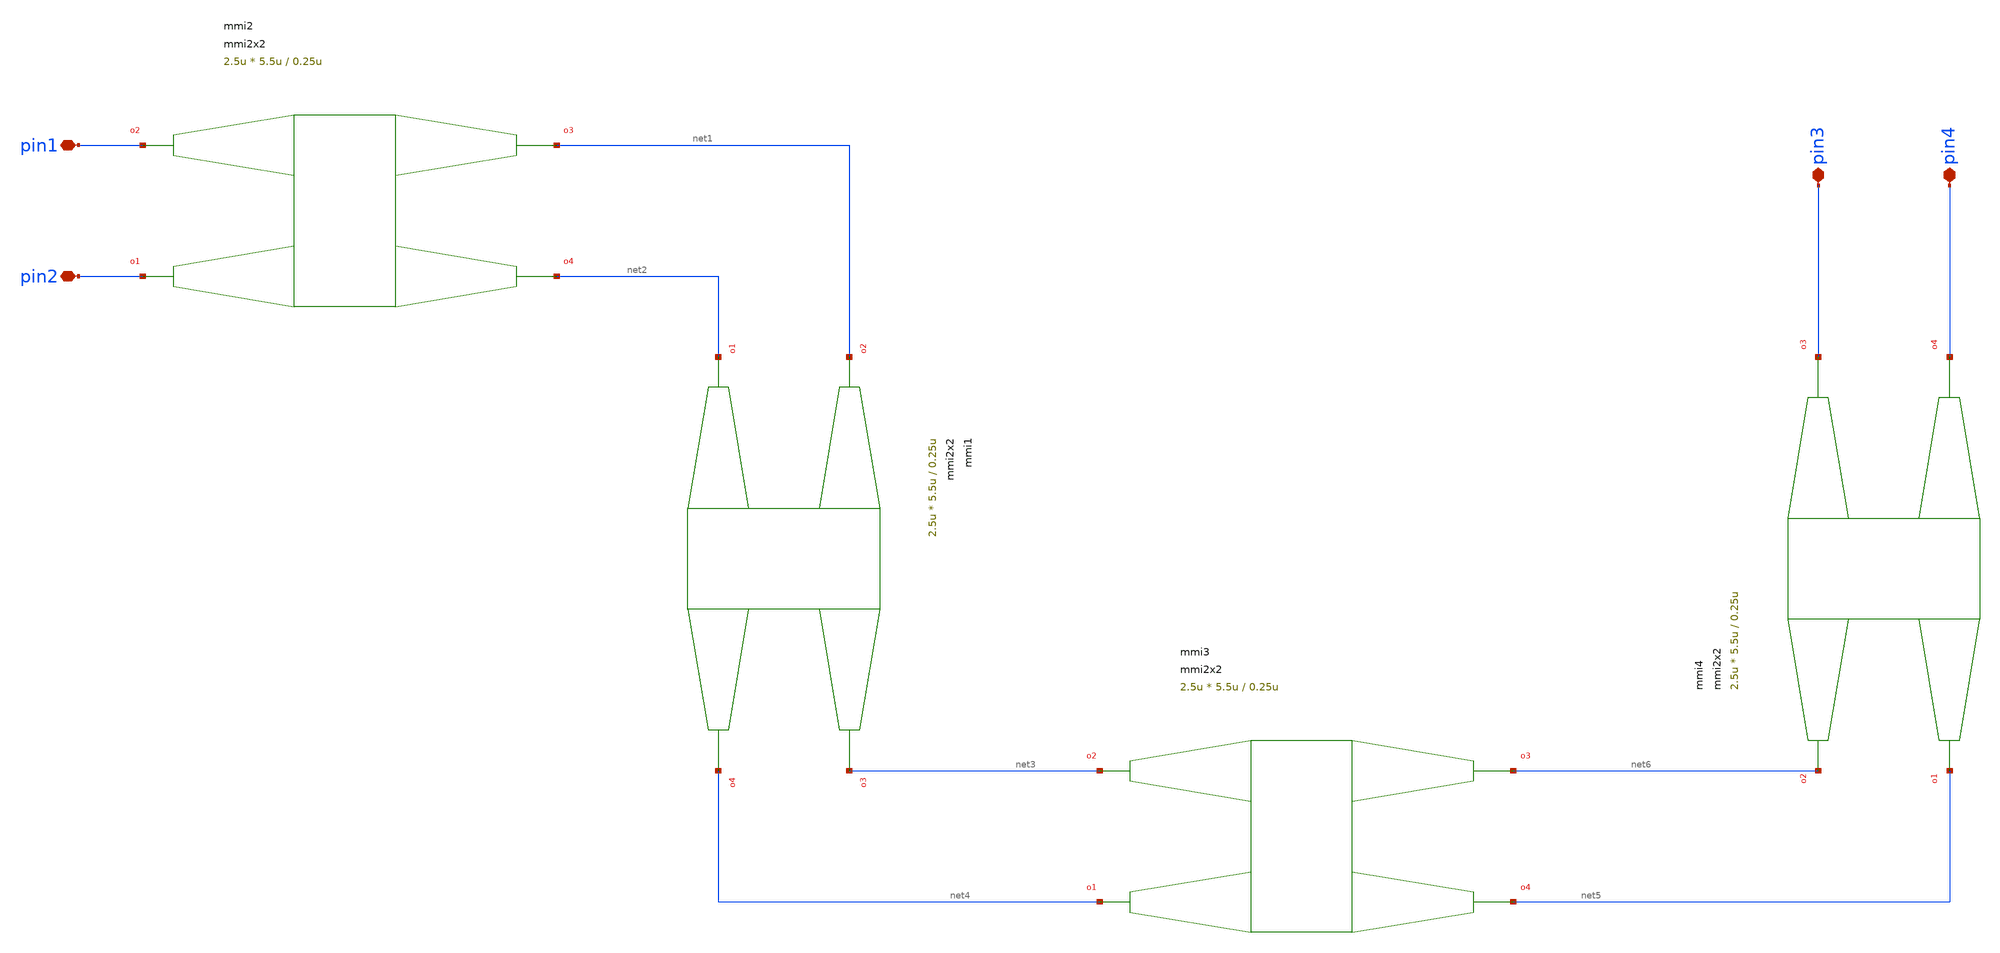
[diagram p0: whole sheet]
** sch_path: xschem/tests/test_sch/test_mmi2x2.sch
* Copyright (c) 2024, Mabrains LLC
* Licensed under the GNU Lesser General Public License, Version 3.0 (the "License");
* you may not use this file except in compliance with the License.
* GNU Lesser General Public License
* Version 3, 29 June 2007
* This program is free software: you can redistribute it and/or modify
* it under the terms of the GNU Lesser General Public License as published
* by the Free Software Foundation, either version 3 of the License, or
* (at your option) any later version.
* This program is distributed in the hope that it will be useful,
* but WITHOUT ANY WARRANTY; without even the implied warranty of
* MERCHANTABILITY or FITNESS FOR A PARTICULAR PURPOSE.  See the
* GNU Lesser General Public License for more details.
* You should have received a copy of the GNU Lesser General Public License
* along with this program.  If not, see <https://www.gnu.org/licenses/>.
* SPDX-License-Identifier: LGPL-3.0
**.subckt test_mmi2x2 pin1 pin2 pin3 pin4
*.iopin pin1
*.iopin pin2
*.iopin pin3
*.iopin pin4
Pmmi2 pin2 pin1 net1 net2 mmi2x2 width=0.5u width_taper=1u length_taper=10u length_mmi=5.5u
+ width_mmi=2.5u gap_mmi=0.25u
Pmmi1 net2 net1 net3 net4 mmi2x2 width=0.5u width_taper=1u length_taper=10u length_mmi=5.5u
+ width_mmi=2.5u gap_mmi=0.25u
Pmmi3 net4 net3 net6 net5 mmi2x2 width=0.5u width_taper=1u length_taper=10u length_mmi=5.5u
+ width_mmi=2.5u gap_mmi=0.25u
Pmmi4 net5 net6 pin3 pin4 mmi2x2 width=0.5u width_taper=1u length_taper=10u length_mmi=5.5u
+ width_mmi=2.5u gap_mmi=0.25u
**.ends
.end
